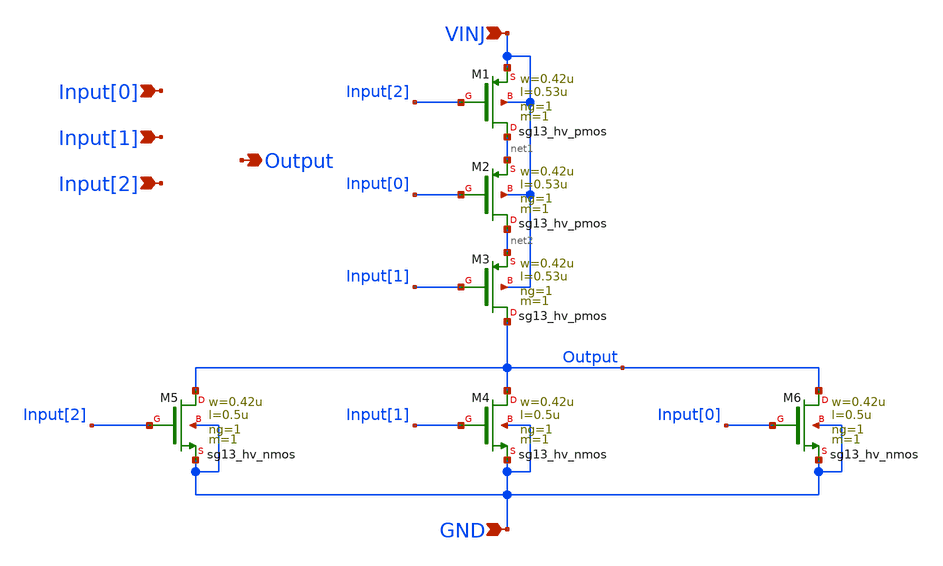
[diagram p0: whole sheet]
** sch_path: ihp130_cells/VinjNOR3/ihp130_VinjNOR3.sch
**.subckt ihp130_VinjNOR3 Input[0] VINJ GND Output Input[1] Input[2]
*.ipin Input[0]
*.ipin VINJ
*.ipin GND
*.opin Output
*.ipin Input[1]
*.ipin Input[2]
XM1 net1 Input[2] VINJ VINJ sg13_hv_pmos w=0.42u l=0.53u ng=1 m=1 mm_ok=1
XM2 net2 Input[0] net1 VINJ sg13_hv_pmos w=0.42u l=0.53u ng=1 m=1 mm_ok=1
XM3 Output Input[1] net2 VINJ sg13_hv_pmos w=0.42u l=0.53u ng=1 m=1 mm_ok=1
XM4 Output Input[1] GND GND sg13_hv_nmos w=0.42u l=0.5u ng=1 m=1 mm_ok=1
XM5 Output Input[2] GND GND sg13_hv_nmos w=0.42u l=0.5u ng=1 m=1 mm_ok=1
XM6 Output Input[0] GND GND sg13_hv_nmos w=0.42u l=0.5u ng=1 m=1 mm_ok=1
**.ends
.end
